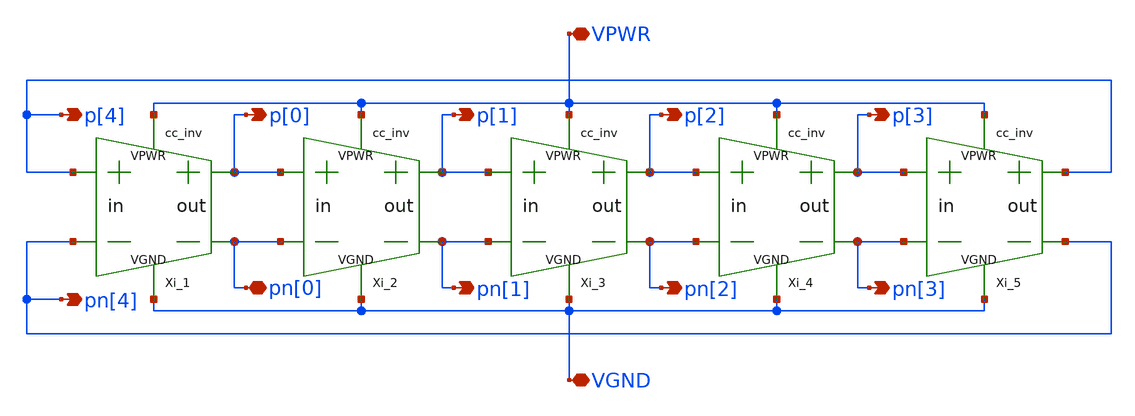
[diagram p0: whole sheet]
** sch_path: xschem/lib/5s_ringOsc.sch
**.subckt 5s_ringOsc VPWR VGND pn[1] p[1] p[2] p[3] p[4] pn[2] pn[3] pn[4] pn[0] p[0]
*.iopin VPWR
*.iopin VGND
*.opin pn[1]
*.opin p[1]
*.opin p[2]
*.opin p[3]
*.opin p[4]
*.opin pn[2]
*.opin pn[3]
*.opin pn[4]
*.iopin pn[0]
*.opin p[0]
Xi_1 p[4] pn[4] VPWR VGND p[0] pn[0] cc_inv L_main="L_main" L_aux="L_aux" Wp="Wp" Wn="Wn"
Xi_2 p[0] pn[0] VPWR VGND p[1] pn[1] cc_inv L_main="L_main" L_aux="L_aux" Wp="Wp" Wn="Wn"
Xi_3 p[1] pn[1] VPWR VGND p[2] pn[2] cc_inv L_main="L_main" L_aux="L_aux" Wp="Wp" Wn="Wn"
Xi_4 p[2] pn[2] VPWR VGND p[3] pn[3] cc_inv L_main="L_main" L_aux="L_aux" Wp="Wp" Wn="Wn"
Xi_5 p[3] pn[3] VPWR VGND p[4] pn[4] cc_inv L_main="L_main" L_aux="L_aux" Wp="Wp" Wn="Wn"
**.ends
.end
